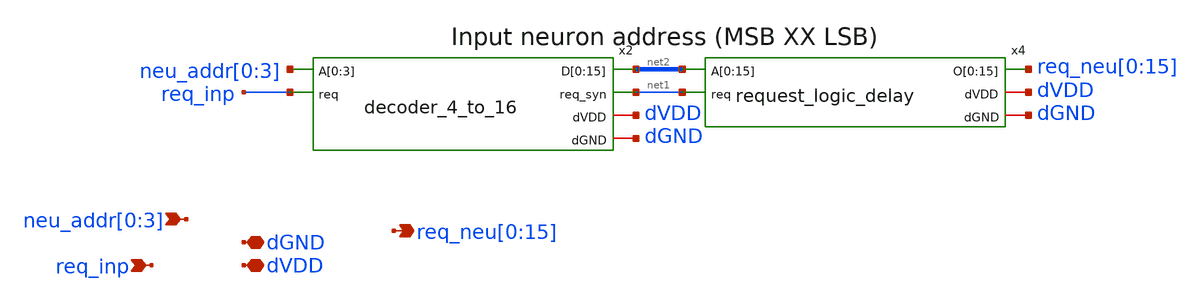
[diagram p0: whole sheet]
** sch_path: design/xschem/input_neuron_address_decoder_16_to_1.sch
**.subckt input_neuron_address_decoder_16_to_1 neu_addr[0],neu_addr[1],neu_addr[2],neu_addr[3]
*+ req_inp dGND dVDD
*+ req_neu[0],req_neu[1],req_neu[2],req_neu[3],req_neu[4],req_neu[5],req_neu[6],req_neu[7],req_neu[8],req_neu[9],req_neu[10],req_neu[11],req_neu[12],req_neu[13],req_neu[14],req_neu[15]
*.ipin neu_addr[0],neu_addr[1],neu_addr[2],neu_addr[3]
*.ipin req_inp
*.iopin dGND
*.iopin dVDD
*.opin
*+ req_neu[0],req_neu[1],req_neu[2],req_neu[3],req_neu[4],req_neu[5],req_neu[6],req_neu[7],req_neu[8],req_neu[9],req_neu[10],req_neu[11],req_neu[12],req_neu[13],req_neu[14],req_neu[15]
x2 neu_addr[0] neu_addr[1] neu_addr[2] neu_addr[3] net2[15] net2[14] net2[13] net2[12] net2[11]
+ net2[10] net2[9] net2[8] net2[7] net2[6] net2[5] net2[4] net2[3] net2[2] net2[1] net2[0] req_inp net1 dVDD
+ dGND decoder_4_to_16
x4 net2[15] net2[14] net2[13] net2[12] net2[11] net2[10] net2[9] net2[8] net2[7] net2[6] net2[5]
+ net2[4] net2[3] net2[2] net2[1] net2[0] req_neu[0] req_neu[1] req_neu[2] req_neu[3] req_neu[4] req_neu[5]
+ req_neu[6] req_neu[7] req_neu[8] req_neu[9] req_neu[10] req_neu[11] req_neu[12] req_neu[13] req_neu[14]
+ req_neu[15] net1 dVDD dGND request_logic_delay
**.ends

* expanding   symbol:  decoder_4_to_16.sym # of pins=6
** sym_path: design/xschem/decoder_4_to_16.sym
** sch_path: design/xschem/decoder_4_to_16.sch
.subckt decoder_4_to_16 A[0] A[1] A[2] A[3] D[0] D[1] D[2] D[3] D[4] D[5] D[6] D[7] D[8] D[9] D[10]
+ D[11] D[12] D[13] D[14] D[15] req req_syn dVDD dGND
*.ipin A[0],A[1],A[2],A[3]
*.ipin req
*.opin D[0],D[1],D[2],D[3],D[4],D[5],D[6],D[7],D[8],D[9],D[10],D[11],D[12],D[13],D[14],D[15]
*.opin req_syn
*.iopin dVDD
*.iopin dGND
x21 req dGND dGND dVDD dVDD net5 sky130_fd_sc_hd__inv_1
x22 net5 dGND dGND dVDD dVDD net6 sky130_fd_sc_hd__inv_1
x23 net6 dGND dGND dVDD dVDD net7 sky130_fd_sc_hd__inv_1
x24 net7 dGND dGND dVDD dVDD req_syn sky130_fd_sc_hd__inv_1
x20 A[3] A[2] A[1] A[0] dGND dGND dVDD dVDD D[15] sky130_fd_sc_hd__and4_1
x19 A[3] A[2] A[1] net4 dGND dGND dVDD dVDD D[14] sky130_fd_sc_hd__and4_1
x18 A[3] A[2] net3 A[0] dGND dGND dVDD dVDD D[13] sky130_fd_sc_hd__and4_1
x17 A[3] A[2] net3 net4 dGND dGND dVDD dVDD D[12] sky130_fd_sc_hd__and4_1
x16 A[3] net2 A[1] A[0] dGND dGND dVDD dVDD D[11] sky130_fd_sc_hd__and4_1
x15 A[3] net2 A[1] net4 dGND dGND dVDD dVDD D[10] sky130_fd_sc_hd__and4_1
x13 A[3] net2 net3 A[0] dGND dGND dVDD dVDD D[9] sky130_fd_sc_hd__and4_1
x4 A[3] net2 net3 net4 dGND dGND dVDD dVDD D[8] sky130_fd_sc_hd__and4_1
x5 net1 A[2] A[1] A[0] dGND dGND dVDD dVDD D[7] sky130_fd_sc_hd__and4_1
x6 net1 A[2] A[1] net4 dGND dGND dVDD dVDD D[6] sky130_fd_sc_hd__and4_1
x8 net1 A[2] net3 net4 dGND dGND dVDD dVDD D[4] sky130_fd_sc_hd__and4_1
x9 net1 net2 A[1] net4 dGND dGND dVDD dVDD D[2] sky130_fd_sc_hd__and4_1
x10 net1 net2 net3 net4 dGND dGND dVDD dVDD D[0] sky130_fd_sc_hd__and4_1
x11 net1 net2 net3 A[0] dGND dGND dVDD dVDD D[1] sky130_fd_sc_hd__and4_1
x12 net1 net2 A[1] A[0] dGND dGND dVDD dVDD D[3] sky130_fd_sc_hd__and4_1
x14 net1 A[2] net3 A[0] dGND dGND dVDD dVDD D[5] sky130_fd_sc_hd__and4_1
x1 A[3] dGND dGND dVDD dVDD net1 sky130_fd_sc_hd__inv_4
x2 A[2] dGND dGND dVDD dVDD net2 sky130_fd_sc_hd__inv_4
x3 A[1] dGND dGND dVDD dVDD net3 sky130_fd_sc_hd__inv_4
x7 A[0] dGND dGND dVDD dVDD net4 sky130_fd_sc_hd__inv_4
.ends


* expanding   symbol:  request_logic_delay.sym # of pins=5
** sym_path: design/xschem/request_logic_delay.sym
** sch_path: design/xschem/request_logic_delay.sch
.subckt request_logic_delay A[0] A[1] A[2] A[3] A[4] A[5] A[6] A[7] A[8] A[9] A[10] A[11] A[12]
+ A[13] A[14] A[15] O[0] O[1] O[2] O[3] O[4] O[5] O[6] O[7] O[8] O[9] O[10] O[11] O[12] O[13] O[14] O[15]
+ req dVDD dGND
*.ipin A[0],A[1],A[2],A[3],A[4],A[5],A[6],A[7],A[8],A[9],A[10],A[11],A[12],A[13],A[14],A[15]
*.ipin req
*.opin O[0],O[1],O[2],O[3],O[4],O[5],O[6],O[7],O[8],O[9],O[10],O[11],O[12],O[13],O[14],O[15]
*.iopin dVDD
*.iopin dGND
x1[0] A[0] req dGND dGND dVDD dVDD O[0] sky130_fd_sc_hd__and2_1
x1[1] A[1] req dGND dGND dVDD dVDD O[1] sky130_fd_sc_hd__and2_1
x1[2] A[2] req dGND dGND dVDD dVDD O[2] sky130_fd_sc_hd__and2_1
x1[3] A[3] req dGND dGND dVDD dVDD O[3] sky130_fd_sc_hd__and2_1
x1[4] A[4] req dGND dGND dVDD dVDD O[4] sky130_fd_sc_hd__and2_1
x1[5] A[5] req dGND dGND dVDD dVDD O[5] sky130_fd_sc_hd__and2_1
x1[6] A[6] req dGND dGND dVDD dVDD O[6] sky130_fd_sc_hd__and2_1
x1[7] A[7] req dGND dGND dVDD dVDD O[7] sky130_fd_sc_hd__and2_1
x1[8] A[8] req dGND dGND dVDD dVDD O[8] sky130_fd_sc_hd__and2_1
x1[9] A[9] req dGND dGND dVDD dVDD O[9] sky130_fd_sc_hd__and2_1
x1[10] A[10] req dGND dGND dVDD dVDD O[10] sky130_fd_sc_hd__and2_1
x1[11] A[11] req dGND dGND dVDD dVDD O[11] sky130_fd_sc_hd__and2_1
x1[12] A[12] req dGND dGND dVDD dVDD O[12] sky130_fd_sc_hd__and2_1
x1[13] A[13] req dGND dGND dVDD dVDD O[13] sky130_fd_sc_hd__and2_1
x1[14] A[14] req dGND dGND dVDD dVDD O[14] sky130_fd_sc_hd__and2_1
x1[15] A[15] req dGND dGND dVDD dVDD O[15] sky130_fd_sc_hd__and2_1
.ends

.end
